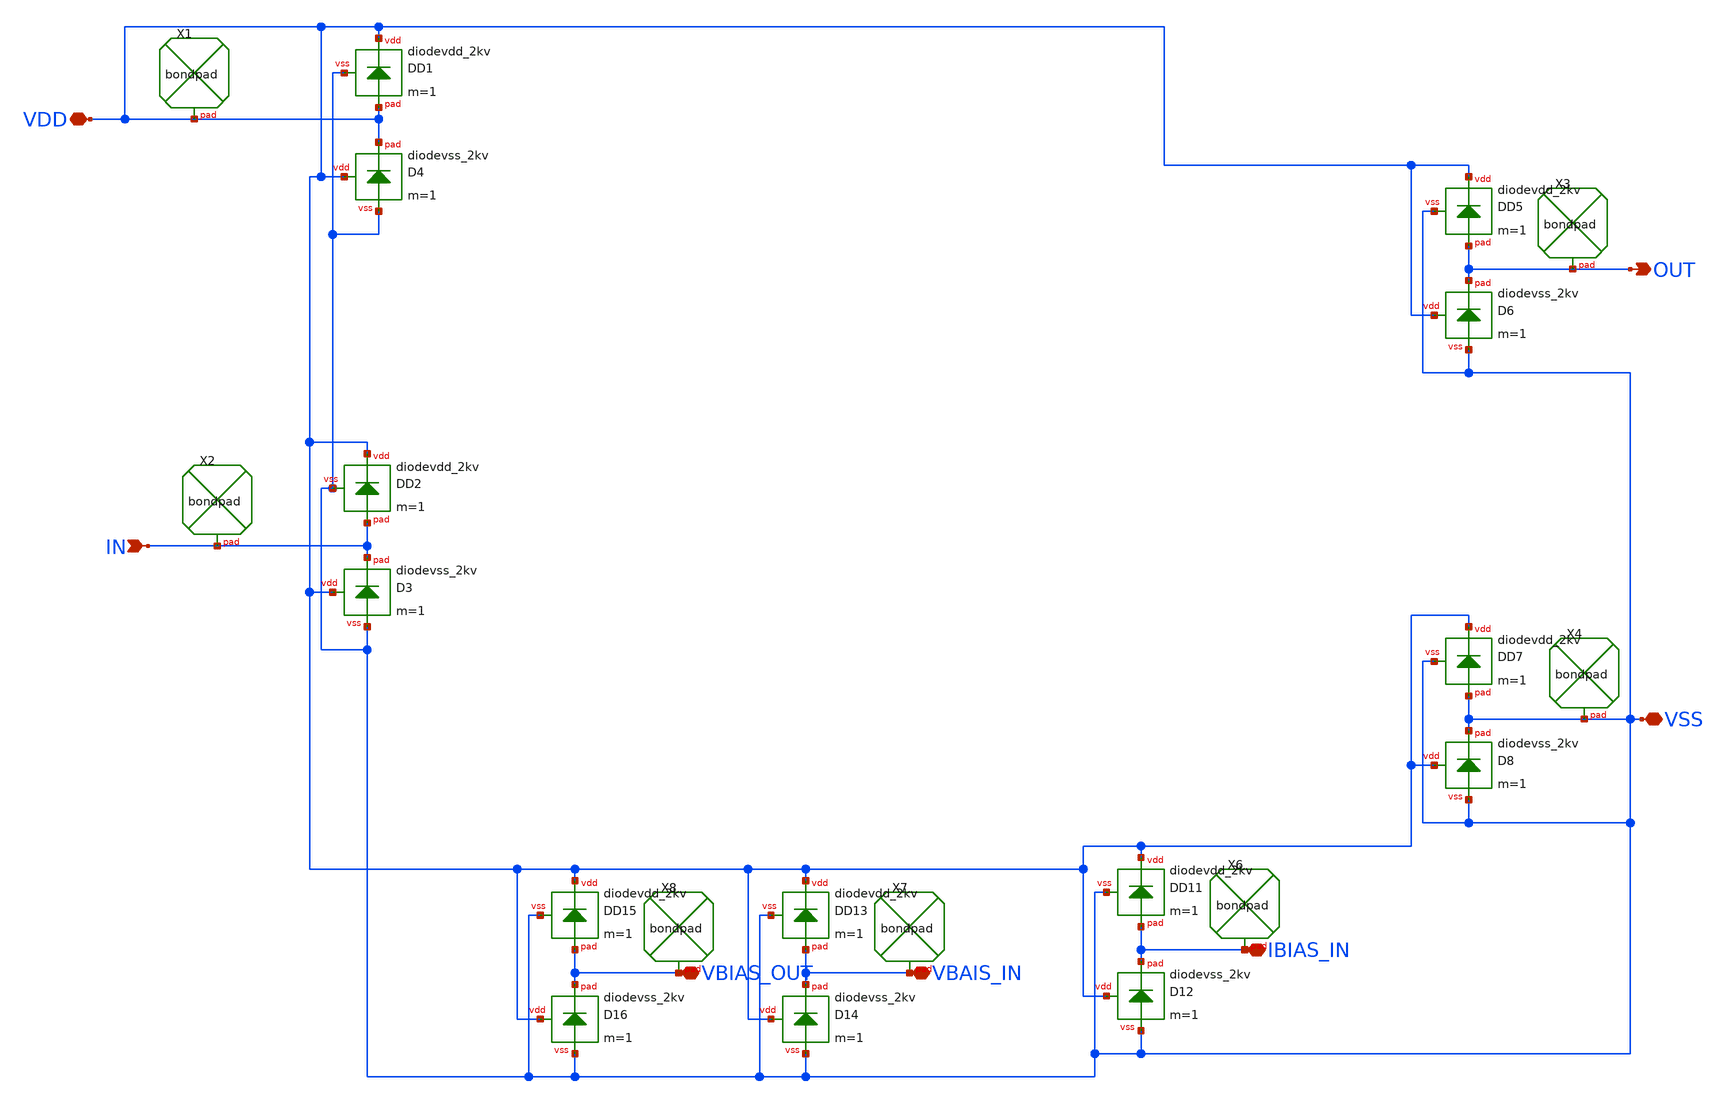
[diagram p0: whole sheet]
** sch_path: GPS_LNA/design_data/lvs/parts/pad_diode_7.sch
**.subckt pad_diode_7 VDD IN OUT VSS VBAIS_IN VBIAS_OUT IBIAS_IN
*.iopin VDD
*.ipin IN
*.opin OUT
*.iopin VSS
*.iopin VBAIS_IN
*.iopin VBIAS_OUT
*.iopin IBIAS_IN
XX1 VDD bondpad size=100u shape=0 padtype=0
XX3 OUT bondpad size=100u shape=0 padtype=0
XX4 VSS bondpad size=100u shape=0 padtype=0
XD1 VDD VDD VSS diodevdd_2kv m=1
XD4 VDD VDD VSS diodevss_2kv m=1
XX2 IN bondpad size=100u shape=0 padtype=0
XD2 VDD IN VSS diodevdd_2kv m=1
XD3 VDD IN VSS diodevss_2kv m=1
XD5 VDD OUT VSS diodevdd_2kv m=1
XD6 VDD OUT VSS diodevss_2kv m=1
XD7 VDD VSS VSS diodevdd_2kv m=1
XD8 VDD VSS VSS diodevss_2kv m=1
XX6 IBIAS_IN bondpad size=100u shape=0 padtype=0
XD11 VDD IBIAS_IN VSS diodevdd_2kv m=1
XD12 VDD IBIAS_IN VSS diodevss_2kv m=1
XX7 VBAIS_IN bondpad size=100u shape=0 padtype=0
XD13 VDD VBAIS_IN VSS diodevdd_2kv m=1
XD14 VDD VBAIS_IN VSS diodevss_2kv m=1
XX8 VBIAS_OUT bondpad size=100u shape=0 padtype=0
XD15 VDD VBIAS_OUT VSS diodevdd_2kv m=1
XD16 VDD VBIAS_OUT VSS diodevss_2kv m=1
**.ends
.end
